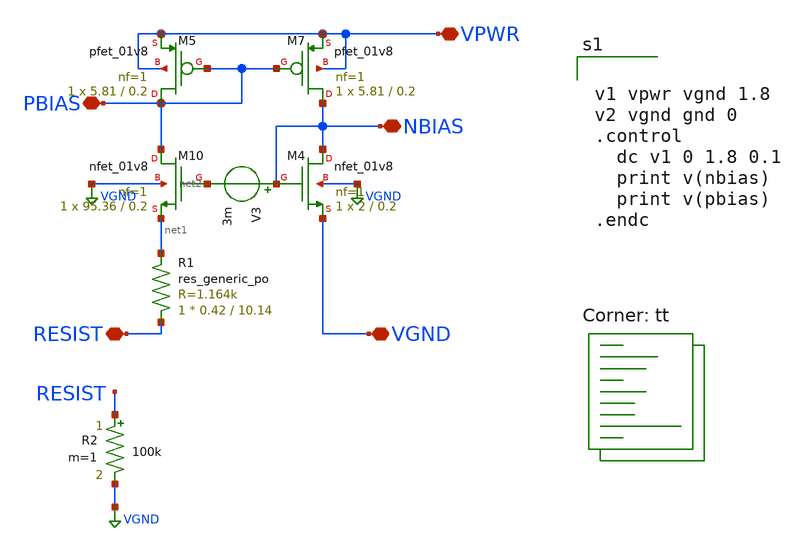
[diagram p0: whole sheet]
** sch_path: project2/bootstrap/bootstrap_mismatch_demo.sch
**.subckt bootstrap_mismatch_demo VPWR NBIAS PBIAS VGND RESIST
*.iopin VPWR
*.iopin NBIAS
*.iopin PBIAS
*.iopin VGND
*.iopin RESIST
XM4 NBIAS NBIAS VGND VGND sky130_fd_pr__nfet_01v8 L=0.2 W=2 nf=1 ad='int((nf+1)/2) * W/nf * 0.29' as='int((nf+2)/2) * W/nf * 0.29'
+ pd='2*int((nf+1)/2) * (W/nf + 0.29)' ps='2*int((nf+2)/2) * (W/nf + 0.29)' nrd='0.29 / W' nrs='0.29 / W'
+ sa=0 sb=0 sd=0 mult=1 m=1
XM7 NBIAS PBIAS VPWR VPWR sky130_fd_pr__pfet_01v8 L=0.2 W=5.81 nf=1 ad='int((nf+1)/2) * W/nf * 0.29'
+ as='int((nf+2)/2) * W/nf * 0.29' pd='2*int((nf+1)/2) * (W/nf + 0.29)' ps='2*int((nf+2)/2) * (W/nf + 0.29)'
+ nrd='0.29 / W' nrs='0.29 / W' sa=0 sb=0 sd=0 mult=1 m=1
XM10 PBIAS net2 net1 VGND sky130_fd_pr__nfet_01v8 L=0.2 W=95.36 nf=1 ad='int((nf+1)/2) * W/nf * 0.29'
+ as='int((nf+2)/2) * W/nf * 0.29' pd='2*int((nf+1)/2) * (W/nf + 0.29)' ps='2*int((nf+2)/2) * (W/nf + 0.29)'
+ nrd='0.29 / W' nrs='0.29 / W' sa=0 sb=0 sd=0 mult=1 m=1
XM5 PBIAS PBIAS VPWR VPWR sky130_fd_pr__pfet_01v8 L=0.2 W=5.81 nf=1 ad='int((nf+1)/2) * W/nf * 0.29'
+ as='int((nf+2)/2) * W/nf * 0.29' pd='2*int((nf+1)/2) * (W/nf + 0.29)' ps='2*int((nf+2)/2) * (W/nf + 0.29)'
+ nrd='0.29 / W' nrs='0.29 / W' sa=0 sb=0 sd=0 mult=1 m=1
XR1 RESIST net1 sky130_fd_pr__res_generic_po W=0.42 L=10.14 m=1
V3 NBIAS net2 3m
R2 RESIST VGND 100k m=1
**** begin user architecture code


v1 vpwr vgnd 1.8
v2 vgnd gnd 0
.control
  dc v1 0 1.8 0.1
  print v(nbias)
  print v(pbias)
.endc


.lib $::SKYWATER_MODELS/sky130.lib.spice tt
**** end user architecture code
**.ends
.GLOBAL VGND
.end
